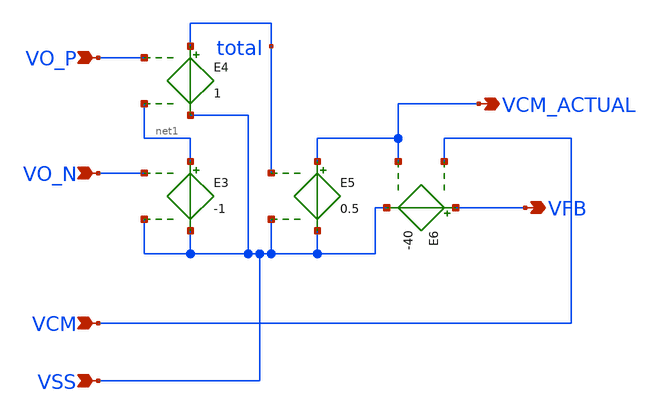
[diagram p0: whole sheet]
** sch_path: cmfb_ideal.sch
**.subckt cmfb_ideal VO_P VO_N VCM VSS VFB VCM_ACTUAL
*.ipin VO_P
*.ipin VO_N
*.ipin VCM
*.ipin VSS
*.opin VFB
*.opin VCM_ACTUAL
E3 net1 VSS VO_N VSS -1
E4 total VSS VO_P net1 1
E5 VCM_ACTUAL VSS total VSS 0.5
E6 VFB VSS VCM VCM_ACTUAL -40
**.ends
.end
